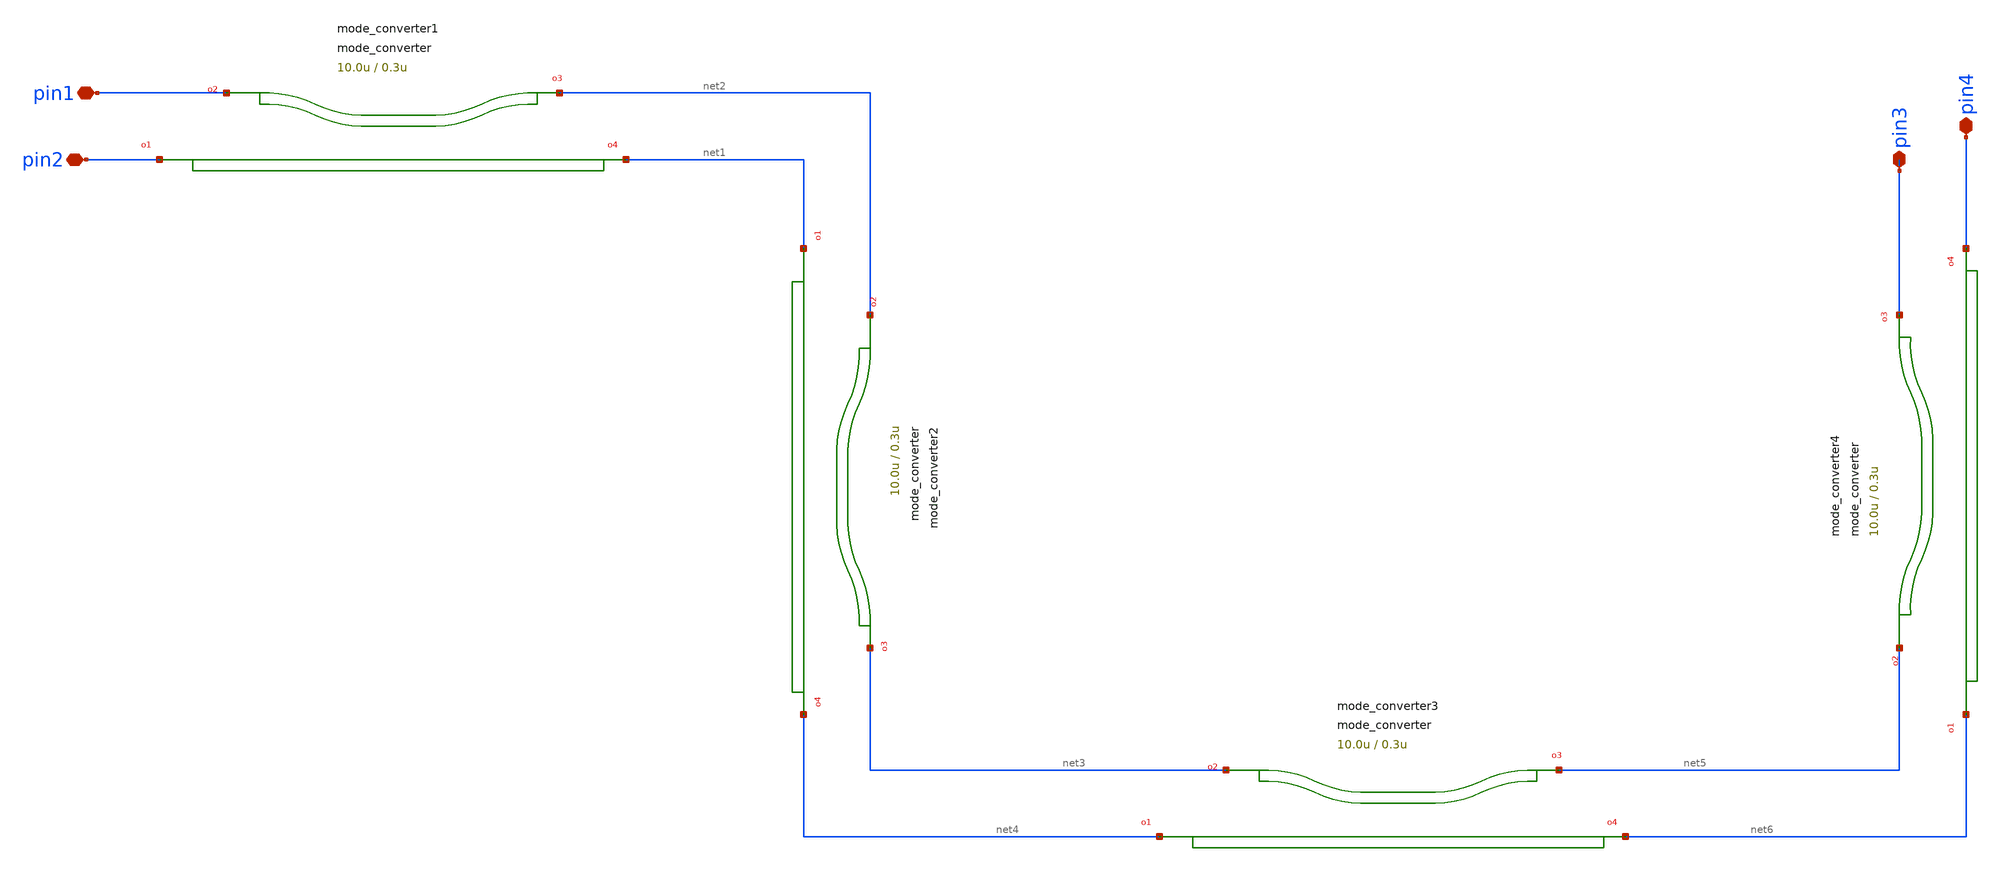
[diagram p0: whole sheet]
** sch_path: xschem/tests/test_sch/test_mode_converter.sch
* Copyright (c) 2024, Mabrains LLC
* Licensed under the GNU Lesser General Public License, Version 3.0 (the "License");
* you may not use this file except in compliance with the License.
* GNU Lesser General Public License
* Version 3, 29 June 2007
* This program is free software: you can redistribute it and/or modify
* it under the terms of the GNU Lesser General Public License as published
* by the Free Software Foundation, either version 3 of the License, or
* (at your option) any later version.
* This program is distributed in the hope that it will be useful,
* but WITHOUT ANY WARRANTY; without even the implied warranty of
* MERCHANTABILITY or FITNESS FOR A PARTICULAR PURPOSE.  See the
* GNU Lesser General Public License for more details.
* You should have received a copy of the GNU Lesser General Public License
* along with this program.  If not, see <https://www.gnu.org/licenses/>.
* SPDX-License-Identifier: LGPL-3.0
**.subckt test_mode_converter pin1 pin2 pin3 pin4
*.iopin pin1
*.iopin pin2
*.iopin pin3
*.iopin pin4
Pmode_converter1 pin2 pin1 net2 net1 mode_converter gap=0.3u length=10.0u mm_width=1.2u
+ mc_mm_width=1.0u sm_width=0.5u
Pmode_converter3 net4 net3 net5 net6 mode_converter gap=0.3u length=10.0u mm_width=1.2u
+ mc_mm_width=1.0u sm_width=0.5u
Pmode_converter4 net6 net5 pin3 pin4 mode_converter gap=0.3u length=10.0u mm_width=1.2u
+ mc_mm_width=1.0u sm_width=0.5u
Pmode_converter2 net1 net2 net3 net4 mode_converter gap=0.3u length=10.0u mm_width=1.2u
+ mc_mm_width=1.0u sm_width=0.5u
**.ends
.end
